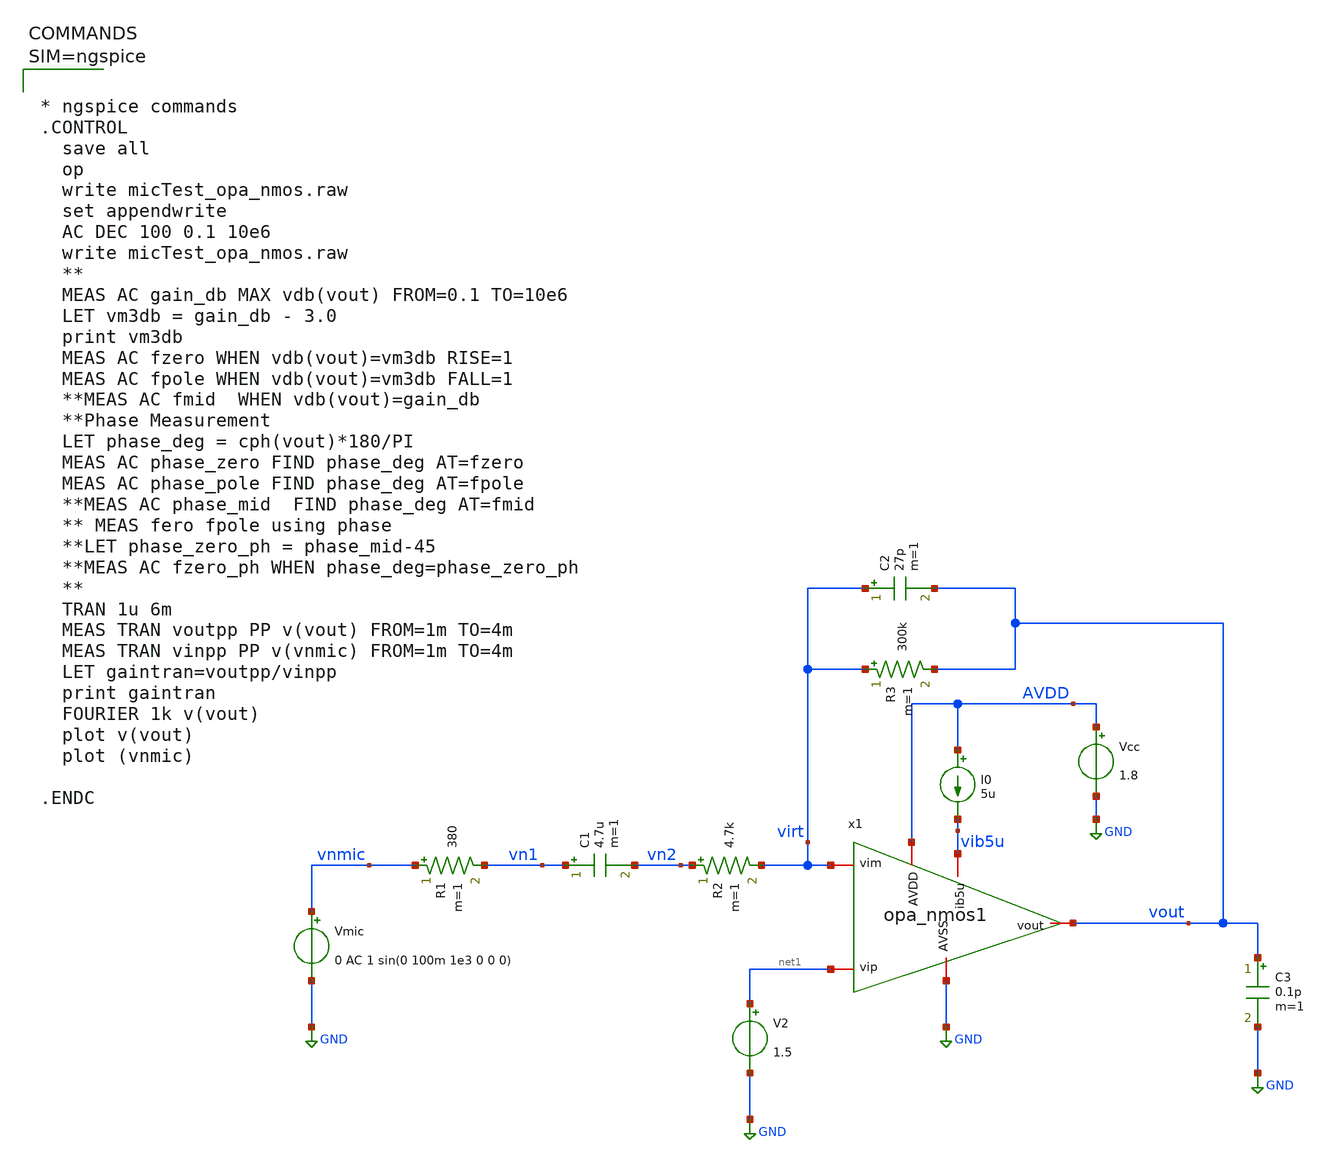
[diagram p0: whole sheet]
** sch_path: xschem/micTest_opa_nmos.sch
**.subckt micTest_opa_nmos
Vmic vnmic GND 0 AC 1 sin(0 100m 1e3 0 0 0)
R1 vnmic vn1 380 m=1
C1 vn1 vn2 4.7u m=1
R2 vn2 virt 4.7k m=1
R3 virt vout 300k m=1
C2 virt vout 27p m=1
V2 net1 GND 1.5
C3 vout GND 0.1p m=1
x1 vout net1 GND virt AVDD vib5u opa_nmos1
Vcc AVDD GND 1.8
I0 AVDD vib5u 5u
**** begin user architecture code



* ngspice commands
.CONTROL
  save all
  op
  write micTest_opa_nmos.raw
  set appendwrite
  AC DEC 100 0.1 10e6
  write micTest_opa_nmos.raw
  **
  MEAS AC gain_db MAX vdb(vout) FROM=0.1 TO=10e6
  LET vm3db = gain_db - 3.0
  print vm3db
  MEAS AC fzero WHEN vdb(vout)=vm3db RISE=1
  MEAS AC fpole WHEN vdb(vout)=vm3db FALL=1
  **MEAS AC fmid  WHEN vdb(vout)=gain_db
  **Phase Measurement
  LET phase_deg = cph(vout)*180/PI
  MEAS AC phase_zero FIND phase_deg AT=fzero
  MEAS AC phase_pole FIND phase_deg AT=fpole
  **MEAS AC phase_mid  FIND phase_deg AT=fmid
  ** MEAS fero fpole using phase
  **LET phase_zero_ph = phase_mid-45
  **MEAS AC fzero_ph WHEN phase_deg=phase_zero_ph
  **
  TRAN 1u 6m
  MEAS TRAN voutpp PP v(vout) FROM=1m TO=4m
  MEAS TRAN vinpp PP v(vnmic) FROM=1m TO=4m
  LET gaintran=voutpp/vinpp
  print gaintran
  FOURIER 1k v(vout)
  plot v(vout)
  plot (vnmic)

.ENDC




** opencircuitdesign pdks install
.lib $::SKYWATER_MODELS/sky130.lib.spice tt

**** end user architecture code
**.ends

* expanding   symbol:  opa_nmos1.sym # of pins=6
** sym_path: xschem/opa_nmos1.sym
** sch_path: xschem/opa_nmos1.sch
.subckt opa_nmos1 vout vip AVSS vim AVDD ib5u
*.iopin vip
*.iopin vim
*.iopin vout
*.iopin ib5u
*.iopin AVDD
*.iopin AVSS
XM1 ib5u ib5u AVSS AVSS sky130_fd_pr__nfet_01v8 L=1 W=5 nf=1 ad='int((1 + 1)/2) * 5 / 1 * 0.29' as='int((1 + 2)/2) * 5 / 1 * 0.29'
+ pd='2*int((1 + 1)/2) * (5 / 1 + 0.29)' ps='2*int((1 + 2)/2) * (5 / 1 + 0.29)' nrd='0.29 / 5 ' nrs='0.29 / 5 '
+ sa=0 sb=0 sd=0 mult=1 m=1
XM2 net1 ib5u AVSS AVSS sky130_fd_pr__nfet_01v8 L=1 W=5 nf=1 ad='int((1 + 1)/2) * 5 / 1 * 0.29' as='int((1 + 2)/2) * 5 / 1 * 0.29'
+ pd='2*int((1 + 1)/2) * (5 / 1 + 0.29)' ps='2*int((1 + 2)/2) * (5 / 1 + 0.29)' nrd='0.29 / 5 ' nrs='0.29 / 5 '
+ sa=0 sb=0 sd=0 mult=2 m=2
XM3 vom vip net1 net1 sky130_fd_pr__nfet_01v8_lvt L=2 W=5 nf=1 ad='int((1 + 1)/2) * 5 / 1 * 0.29' as='int((1 + 2)/2) * 5 / 1 * 0.29'
+ pd='2*int((1 + 1)/2) * (5 / 1 + 0.29)' ps='2*int((1 + 2)/2) * (5 / 1 + 0.29)' nrd='0.29 / 5 ' nrs='0.29 / 5 '
+ sa=0 sb=0 sd=0 mult=4 m=4
XM4 vout vim net1 net1 sky130_fd_pr__nfet_01v8_lvt L=2 W=4 nf=1 ad='int((1 + 1)/2) * 4 / 1 * 0.29' as='int((1 + 2)/2) * 4 / 1 * 0.29'
+ pd='2*int((1 + 1)/2) * (4 / 1 + 0.29)' ps='2*int((1 + 2)/2) * (4 / 1 + 0.29)' nrd='0.29 / 4 ' nrs='0.29 / 4 '
+ sa=0 sb=0 sd=0 mult=5 m=5
XM11 vom vom AVDD AVDD sky130_fd_pr__pfet_01v8 L=2 W=5 nf=1 ad='int((nf+1)/2) * W/nf * 0.29' as='int((nf+2)/2) * W/nf * 0.29'
+ pd='2*int((nf+1)/2) * (W/nf + 0.29)' ps='2*int((nf+2)/2) * (W/nf + 0.29)' nrd='0.29 / W' nrs='0.29 / W'
+ sa=0 sb=0 sd=0 mult=2 m=2
XM5 vout vom AVDD AVDD sky130_fd_pr__pfet_01v8 L=2 W=5 nf=1 ad='int((nf+1)/2) * W/nf * 0.29' as='int((nf+2)/2) * W/nf * 0.29'
+ pd='2*int((nf+1)/2) * (W/nf + 0.29)' ps='2*int((nf+2)/2) * (W/nf + 0.29)' nrd='0.29 / W' nrs='0.29 / W'
+ sa=0 sb=0 sd=0 mult=2 m=2
**** begin user architecture code



* ngspice commands




**** end user architecture code
.ends

.GLOBAL GND
.end
